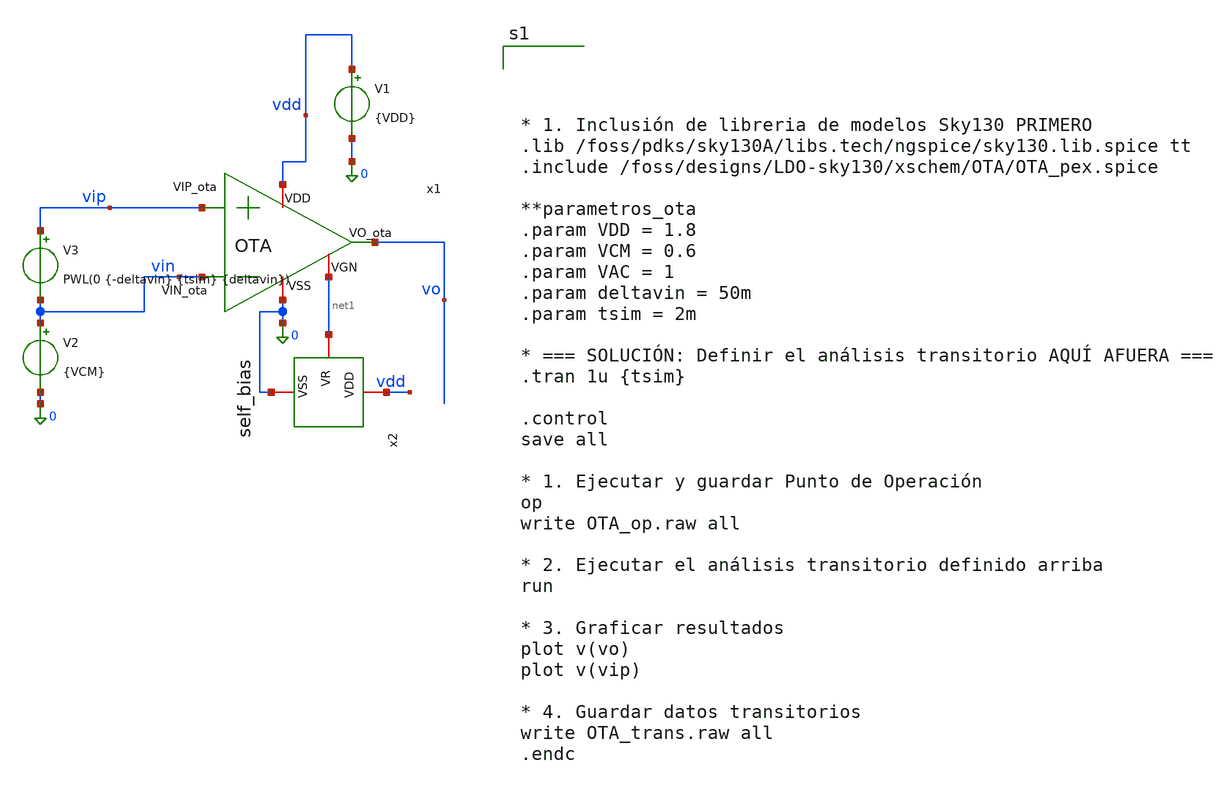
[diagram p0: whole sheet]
** sch_path: xschem/OTA/OTA_tbtran.sch
**.subckt OTA_tbtran
x1 vdd vo vin vip 0 net1 OTA
V1 vdd 0 {VDD}
V2 vin 0 {VCM}
V3 vip vin PWL(0 {-deltavin} {tsim} {deltavin})
x2 vdd net1 0 self_bias
**** begin user architecture code




* 1. Inclusión de libreria de modelos Sky130 PRIMERO
.lib /foss/pdks/sky130A/libs.tech/ngspice/sky130.lib.spice tt
.include /foss/designs/LDO-sky130/xschem/OTA/OTA_pex.spice

**parametros_ota
.param VDD = 1.8
.param VCM = 0.6
.param VAC = 1
.param deltavin = 50m
.param tsim = 2m

* === SOLUCIÓN: Definir el análisis transitorio AQUÍ AFUERA ===
.tran 1u {tsim}

.control
save all

* 1. Ejecutar y guardar Punto de Operación
op
write OTA_op.raw all

* 2. Ejecutar el análisis transitorio definido arriba
run

* 3. Graficar resultados
plot v(vo)
plot v(vip)

* 4. Guardar datos transitorios
write OTA_trans.raw all
.endc



**** end user architecture code
**.ends

* expanding   symbol:  /foss/designs/LDO-sky130/xschem/OTA/OTA.sym # of pins=6
** sym_path: xschem/OTA/OTA.sym
** sch_path: xschem/OTA/OTA.sch
.subckt OTA VDD VO_ota VIN_ota VIP_ota VSS VGN
*.ipin VIN_ota
*.opin VO_ota
*.iopin VSS
*.iopin VDD
*.ipin VIP_ota
*.iopin VGN
XMpr vo1 vd VSS VSS sky130_fd_pr__nfet_01v8 L=1 W=6 nf=4 ad='int((4 + 1)/2) * 6 / 4 * 0.29' as='int((4 + 2)/2) * 6 / 4 * 0.29'
+ pd='2*int((4 + 1)/2) * (6 / 4 + 0.29)' ps='2*int((4 + 2)/2) * (6 / 4 + 0.29)' nrd='0.29 / 6 ' nrs='0.29 / 6 '
+ sa=0 sb=0 sd=0 mult=1 m=1
XMnr vd vd VSS VSS sky130_fd_pr__nfet_01v8 L=1 W=6 nf=4 ad='int((4 + 1)/2) * 6 / 4 * 0.29' as='int((4 + 2)/2) * 6 / 4 * 0.29'
+ pd='2*int((4 + 1)/2) * (6 / 4 + 0.29)' ps='2*int((4 + 2)/2) * (6 / 4 + 0.29)' nrd='0.29 / 6 ' nrs='0.29 / 6 '
+ sa=0 sb=0 sd=0 mult=1 m=1
XMo VO_ota vo1 VSS VSS sky130_fd_pr__nfet_01v8 L=2 W=8 nf=8 ad='int((8 + 1)/2) * 8 / 8 * 0.29' as='int((8 + 2)/2) * 8 / 8 * 0.29'
+ pd='2*int((8 + 1)/2) * (8 / 8 + 0.29)' ps='2*int((8 + 2)/2) * (8 / 8 + 0.29)' nrd='0.29 / 8 ' nrs='0.29 / 8 '
+ sa=0 sb=0 sd=0 mult=1 m=1
XMrc2 VO_ota vgp VDD VDD sky130_fd_pr__pfet_01v8_lvt L=2 W=50 nf=8 ad='int((8 + 1)/2) * 50 / 8 * 0.29'
+ as='int((8 + 2)/2) * 50 / 8 * 0.29' pd='2*int((8 + 1)/2) * (50 / 8 + 0.29)' ps='2*int((8 + 2)/2) * (50 / 8 + 0.29)'
+ nrd='0.29 / 50 ' nrs='0.29 / 50 ' sa=0 sb=0 sd=0 mult=1 m=1
XC1 VO_ota vmiler sky130_fd_pr__cap_mim_m3_2 W=44.6 L=56 MF=1 m=1
XMp vo1 VIP_ota vtail VDD sky130_fd_pr__pfet_01v8_lvt L=1 W=26 nf=4 ad='int((4 + 1)/2) * 26 / 4 * 0.29'
+ as='int((4 + 2)/2) * 26 / 4 * 0.29' pd='2*int((4 + 1)/2) * (26 / 4 + 0.29)' ps='2*int((4 + 2)/2) * (26 / 4 + 0.29)'
+ nrd='0.29 / 26 ' nrs='0.29 / 26 ' sa=0 sb=0 sd=0 mult=1 m=1
XMn vd VIN_ota vtail VDD sky130_fd_pr__pfet_01v8_lvt L=1 W=26 nf=4 ad='int((4 + 1)/2) * 26 / 4 * 0.29'
+ as='int((4 + 2)/2) * 26 / 4 * 0.29' pd='2*int((4 + 1)/2) * (26 / 4 + 0.29)' ps='2*int((4 + 2)/2) * (26 / 4 + 0.29)'
+ nrd='0.29 / 26 ' nrs='0.29 / 26 ' sa=0 sb=0 sd=0 mult=1 m=1
XMrc1 vtail vgp VDD VDD sky130_fd_pr__pfet_01v8_lvt L=1 W=50 nf=8 ad='int((8 + 1)/2) * 50 / 8 * 0.29'
+ as='int((8 + 2)/2) * 50 / 8 * 0.29' pd='2*int((8 + 1)/2) * (50 / 8 + 0.29)' ps='2*int((8 + 2)/2) * (50 / 8 + 0.29)'
+ nrd='0.29 / 50 ' nrs='0.29 / 50 ' sa=0 sb=0 sd=0 mult=1 m=1
XMr vgp vgp VDD VDD sky130_fd_pr__pfet_01v8_lvt L=1 W=12.5 nf=2 ad='int((2 + 1)/2) * 12.5 / 2 * 0.29'
+ as='int((2 + 2)/2) * 12.5 / 2 * 0.29' pd='2*int((2 + 1)/2) * (12.5 / 2 + 0.29)' ps='2*int((2 + 2)/2) * (12.5 / 2 + 0.29)'
+ nrd='0.29 / 12.5 ' nrs='0.29 / 12.5 ' sa=0 sb=0 sd=0 mult=1 m=1
XMnref vgp VGN VSS VSS sky130_fd_pr__nfet_01v8 L=1 W=8 nf=1 ad='int((1 + 1)/2) * 8 / 1 * 0.29' as='int((1 + 2)/2) * 8 / 1 * 0.29'
+ pd='2*int((1 + 1)/2) * (8 / 1 + 0.29)' ps='2*int((1 + 2)/2) * (8 / 1 + 0.29)' nrd='0.29 / 8 ' nrs='0.29 / 8 '
+ sa=0 sb=0 sd=0 mult=1 m=1
XR10 vo1 vmiler VSS sky130_fd_pr__res_xhigh_po_0p35 L=90.72 mult=1 m=1
.ends


* expanding   symbol:  /foss/designs/LDO-sky130/xschem/Self_Bias/self_bias.sym # of pins=3
** sym_path: xschem/Iref/self_bias.sym
** sch_path: xschem/Iref/self_bias.sch
.subckt self_bias VDD VR VSS
*.iopin VR
*.iopin VDD
*.iopin VSS
XMp4 vgp_self vgp_self VDD VDD sky130_fd_pr__pfet_01v8_lvt L=1 W=30 nf=6 ad='int((6 + 1)/2) * 30 / 6 * 0.29'
+ as='int((6 + 2)/2) * 30 / 6 * 0.29' pd='2*int((6 + 1)/2) * (30 / 6 + 0.29)' ps='2*int((6 + 2)/2) * (30 / 6 + 0.29)'
+ nrd='0.29 / 30 ' nrs='0.29 / 30 ' sa=0 sb=0 sd=0 mult=1 m=1
XMp3 VDI vgp_self VDD VDD sky130_fd_pr__pfet_01v8_lvt L=1 W=30 nf=6 ad='int((6 + 1)/2) * 30 / 6 * 0.29'
+ as='int((6 + 2)/2) * 30 / 6 * 0.29' pd='2*int((6 + 1)/2) * (30 / 6 + 0.29)' ps='2*int((6 + 2)/2) * (30 / 6 + 0.29)'
+ nrd='0.29 / 30 ' nrs='0.29 / 30 ' sa=0 sb=0 sd=0 mult=1 m=1
XMs2 VDinv VR vp1 VDD sky130_fd_pr__pfet_01v8_lvt L=5 W=0.5 nf=1 ad='int((1 + 1)/2) * 0.5 / 1 * 0.29'
+ as='int((1 + 2)/2) * 0.5 / 1 * 0.29' pd='2*int((1 + 1)/2) * (0.5 / 1 + 0.29)' ps='2*int((1 + 2)/2) * (0.5 / 1 + 0.29)'
+ nrd='0.29 / 0.5 ' nrs='0.29 / 0.5 ' sa=0 sb=0 sd=0 mult=1 m=1
XMn2 vgp_self VDI VR VSS sky130_fd_pr__nfet_01v8 L=1 W=24 nf=6 ad='int((6 + 1)/2) * 24 / 6 * 0.29' as='int((6 + 2)/2) * 24 / 6 * 0.29'
+ pd='2*int((6 + 1)/2) * (24 / 6 + 0.29)' ps='2*int((6 + 2)/2) * (24 / 6 + 0.29)' nrd='0.29 / 24 ' nrs='0.29 / 24 '
+ sa=0 sb=0 sd=0 mult=1 m=1
XMn1 VDI VR VSS VSS sky130_fd_pr__nfet_01v8 L=1 W=5 nf=5 ad='int((5 + 1)/2) * 5 / 5 * 0.29' as='int((5 + 2)/2) * 5 / 5 * 0.29'
+ pd='2*int((5 + 1)/2) * (5 / 5 + 0.29)' ps='2*int((5 + 2)/2) * (5 / 5 + 0.29)' nrd='0.29 / 5 ' nrs='0.29 / 5 '
+ sa=0 sb=0 sd=0 mult=1 m=1
XMs3 VDinv VR VSS VSS sky130_fd_pr__nfet_01v8 L=1 W=20 nf=5 ad='int((5 + 1)/2) * 20 / 5 * 0.29' as='int((5 + 2)/2) * 20 / 5 * 0.29'
+ pd='2*int((5 + 1)/2) * (20 / 5 + 0.29)' ps='2*int((5 + 2)/2) * (20 / 5 + 0.29)' nrd='0.29 / 20 ' nrs='0.29 / 20 '
+ sa=0 sb=0 sd=0 mult=1 m=1
XMs1 vgp_self VDinv VSS VSS sky130_fd_pr__nfet_01v8 L=1 W=2 nf=2 ad='int((2 + 1)/2) * 2 / 2 * 0.29' as='int((2 + 2)/2) * 2 / 2 * 0.29'
+ pd='2*int((2 + 1)/2) * (2 / 2 + 0.29)' ps='2*int((2 + 2)/2) * (2 / 2 + 0.29)' nrd='0.29 / 2 ' nrs='0.29 / 2 '
+ sa=0 sb=0 sd=0 mult=1 m=1
XR11 VSS VR VSS sky130_fd_pr__res_xhigh_po_0p69 L=20.7 mult=1 m=1
XMs4 vp1 VR vp2 VDD sky130_fd_pr__pfet_01v8_lvt L=5 W=0.5 nf=1 ad='int((1 + 1)/2) * 0.5 / 1 * 0.29' as='int((1 + 2)/2) * 0.5 / 1 * 0.29'
+ pd='2*int((1 + 1)/2) * (0.5 / 1 + 0.29)' ps='2*int((1 + 2)/2) * (0.5 / 1 + 0.29)' nrd='0.29 / 0.5 ' nrs='0.29 / 0.5 '
+ sa=0 sb=0 sd=0 mult=1 m=1
XMs5 vp2 VR vp3 VDD sky130_fd_pr__pfet_01v8_lvt L=5 W=0.5 nf=1 ad='int((1 + 1)/2) * 0.5 / 1 * 0.29' as='int((1 + 2)/2) * 0.5 / 1 * 0.29'
+ pd='2*int((1 + 1)/2) * (0.5 / 1 + 0.29)' ps='2*int((1 + 2)/2) * (0.5 / 1 + 0.29)' nrd='0.29 / 0.5 ' nrs='0.29 / 0.5 '
+ sa=0 sb=0 sd=0 mult=1 m=1
XMs6 vp3 VR vp4 VDD sky130_fd_pr__pfet_01v8_lvt L=5 W=0.5 nf=1 ad='int((1 + 1)/2) * 0.5 / 1 * 0.29' as='int((1 + 2)/2) * 0.5 / 1 * 0.29'
+ pd='2*int((1 + 1)/2) * (0.5 / 1 + 0.29)' ps='2*int((1 + 2)/2) * (0.5 / 1 + 0.29)' nrd='0.29 / 0.5 ' nrs='0.29 / 0.5 '
+ sa=0 sb=0 sd=0 mult=1 m=1
XMs7 vp4 VR VDD VDD sky130_fd_pr__pfet_01v8_lvt L=5 W=0.5 nf=1 ad='int((1 + 1)/2) * 0.5 / 1 * 0.29' as='int((1 + 2)/2) * 0.5 / 1 * 0.29'
+ pd='2*int((1 + 1)/2) * (0.5 / 1 + 0.29)' ps='2*int((1 + 2)/2) * (0.5 / 1 + 0.29)' nrd='0.29 / 0.5 ' nrs='0.29 / 0.5 '
+ sa=0 sb=0 sd=0 mult=1 m=1
.ends

.end
